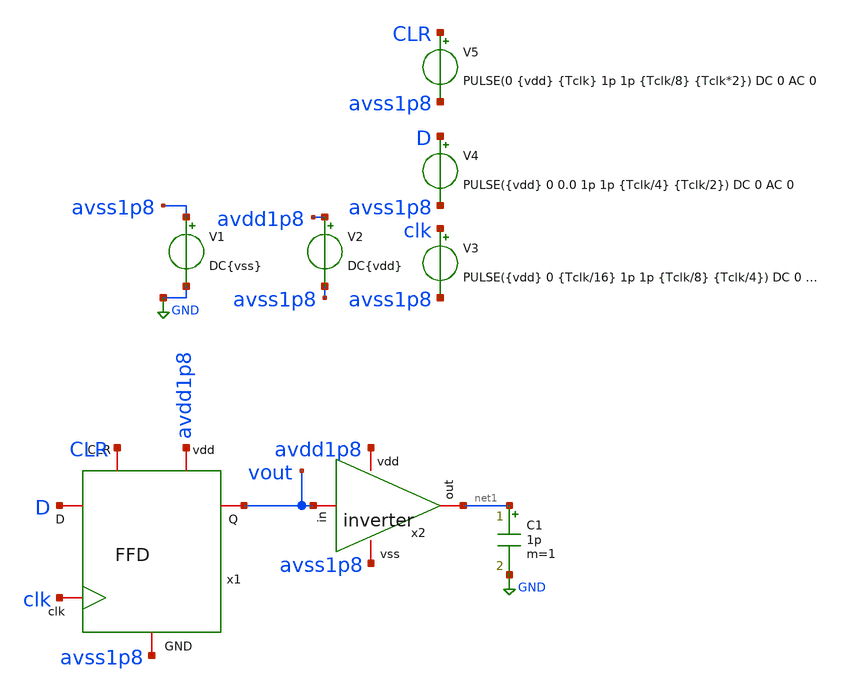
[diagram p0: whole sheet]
** sch_path: simbolos y esquematicos/tb_FFD.sch
**.subckt tb_FFD
V3 clk avss1p8 PULSE({vdd} 0 {Tclk/16} 1p 1p {Tclk/8} {Tclk/4}) DC 0 AC 0
V1 avss1p8 GND DC{vss}
V2 avdd1p8 avss1p8 DC{vdd}
x2 avdd1p8 vout net1 avss1p8 inverter
C1 net1 GND 1p m=1
V4 D avss1p8 PULSE({vdd} 0 0.0 1p 1p {Tclk/4} {Tclk/2}) DC 0 AC 0
x1 avdd1p8 avss1p8 CLR vout D clk FFD
V5 CLR avss1p8 PULSE(0 {vdd} {Tclk} 1p 1p {Tclk/8} {Tclk*2}) DC 0 AC 0
**** begin user architecture code


* Circuit Parameters
.param vdd= 1.8
.param vss= 0.0
.param Tclk = 50n
.options TEMP = 65.0
* Include Models
.lib /foss/pdks/sky130A/libs.tech/ngspice/sky130.lib.spice TT
* OP Parameters & Singals to save
.save all
*Simulations
.control
tran 0.01u 100n
setplot tran1
plot v(clk) v(D)+2 v(CLR)+4 v(vout)+6
.endc
.end


**** end user architecture code
**.ends
.GLOBAL GND
.end
